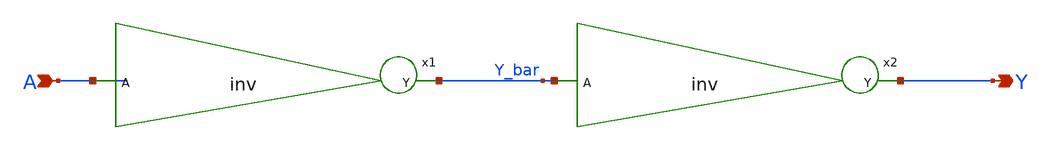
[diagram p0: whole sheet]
** sch_path: eng331lab_final/eng331lab_xschem/buffer.sch
**.subckt buffer A Y
*.ipin A
*.opin Y
x1 Y_bar A inv
x2 Y Y_bar inv
**.ends

* expanding   symbol:  /home/student/xschem_sky130/eng331lab_xschem/inv.sym # of pins=2
** sym_path: eng331lab_final/eng331lab_xschem/inv.sym
** sch_path: eng331lab_final/eng331lab_xschem/inv.sch
.subckt inv Y A
*.ipin A
*.opin Y
XM1 Y A VDD VDD sky130_fd_pr__pfet_01v8 L=0.15 W=0.8 nf=1 ad='int((1 + 1)/2) * 0.8 / 1 * 0.29' as='int((1 + 2)/2) * 0.8 / 1 * 0.29'
+ pd='2*int((1 + 1)/2) * (0.8 / 1 + 0.29)' ps='2*int((1 + 2)/2) * (0.8 / 1 + 0.29)' nrd='0.29 / 0.8 ' nrs='0.29 / 0.8 '
+ sa=0 sb=0 sd=0 mult=1 m=1
XM2 Y A GND GND sky130_fd_pr__nfet_01v8 L=0.15 W=0.5 nf=1 ad='int((1 + 1)/2) * 0.5 / 1 * 0.29' as='int((1 + 2)/2) * 0.5 / 1 * 0.29'
+ pd='2*int((1 + 1)/2) * (0.5 / 1 + 0.29)' ps='2*int((1 + 2)/2) * (0.5 / 1 + 0.29)' nrd='0.29 / 0.5 ' nrs='0.29 / 0.5 '
+ sa=0 sb=0 sd=0 mult=1 m=1
.ends

.GLOBAL VDD
.GLOBAL GND
.end
